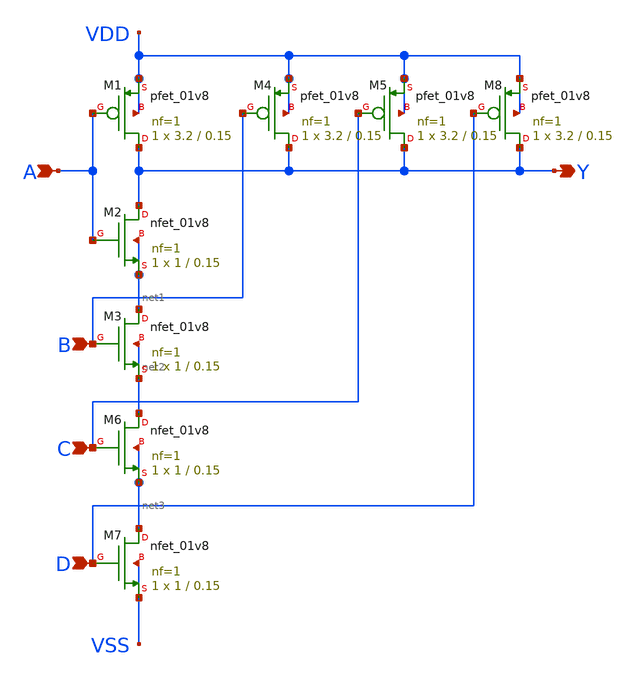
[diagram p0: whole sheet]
** sch_path: design/xschem/NAND/nand4.sch
**.subckt nand4 A Y B C D
*.ipin A
*.opin Y
*.ipin B
*.ipin C
*.ipin D
XM1 Y A VDD VDD sky130_fd_pr__pfet_01v8 L=0.15 W=3.2 nf=1 ad='int((nf+1)/2) * W/nf * 0.29' as='int((nf+2)/2) * W/nf * 0.29'
+ pd='2*int((nf+1)/2) * (W/nf + 0.29)' ps='2*int((nf+2)/2) * (W/nf + 0.29)' nrd='0.29 / W' nrs='0.29 / W'
+ sa=0 sb=0 sd=0 mult=1 m=1
XM2 Y A net1 net1 sky130_fd_pr__nfet_01v8 L=0.15 W=1 nf=1 ad='int((nf+1)/2) * W/nf * 0.29' as='int((nf+2)/2) * W/nf * 0.29'
+ pd='2*int((nf+1)/2) * (W/nf + 0.29)' ps='2*int((nf+2)/2) * (W/nf + 0.29)' nrd='0.29 / W' nrs='0.29 / W'
+ sa=0 sb=0 sd=0 mult=1 m=1
XM3 net1 B net2 net2 sky130_fd_pr__nfet_01v8 L=0.15 W=1 nf=1 ad='int((nf+1)/2) * W/nf * 0.29' as='int((nf+2)/2) * W/nf * 0.29'
+ pd='2*int((nf+1)/2) * (W/nf + 0.29)' ps='2*int((nf+2)/2) * (W/nf + 0.29)' nrd='0.29 / W' nrs='0.29 / W'
+ sa=0 sb=0 sd=0 mult=1 m=1
XM4 Y B VDD VDD sky130_fd_pr__pfet_01v8 L=0.15 W=3.2 nf=1 ad='int((nf+1)/2) * W/nf * 0.29' as='int((nf+2)/2) * W/nf * 0.29'
+ pd='2*int((nf+1)/2) * (W/nf + 0.29)' ps='2*int((nf+2)/2) * (W/nf + 0.29)' nrd='0.29 / W' nrs='0.29 / W'
+ sa=0 sb=0 sd=0 mult=1 m=1
XM5 Y C VDD VDD sky130_fd_pr__pfet_01v8 L=0.15 W=3.2 nf=1 ad='int((nf+1)/2) * W/nf * 0.29' as='int((nf+2)/2) * W/nf * 0.29'
+ pd='2*int((nf+1)/2) * (W/nf + 0.29)' ps='2*int((nf+2)/2) * (W/nf + 0.29)' nrd='0.29 / W' nrs='0.29 / W'
+ sa=0 sb=0 sd=0 mult=1 m=1
XM6 net2 C net3 net3 sky130_fd_pr__nfet_01v8 L=0.15 W=1 nf=1 ad='int((nf+1)/2) * W/nf * 0.29' as='int((nf+2)/2) * W/nf * 0.29'
+ pd='2*int((nf+1)/2) * (W/nf + 0.29)' ps='2*int((nf+2)/2) * (W/nf + 0.29)' nrd='0.29 / W' nrs='0.29 / W'
+ sa=0 sb=0 sd=0 mult=1 m=1
XM7 net3 D VSS VSS sky130_fd_pr__nfet_01v8 L=0.15 W=1 nf=1 ad='int((nf+1)/2) * W/nf * 0.29' as='int((nf+2)/2) * W/nf * 0.29'
+ pd='2*int((nf+1)/2) * (W/nf + 0.29)' ps='2*int((nf+2)/2) * (W/nf + 0.29)' nrd='0.29 / W' nrs='0.29 / W'
+ sa=0 sb=0 sd=0 mult=1 m=1
XM8 Y D VDD VDD sky130_fd_pr__pfet_01v8 L=0.15 W=3.2 nf=1 ad='int((nf+1)/2) * W/nf * 0.29' as='int((nf+2)/2) * W/nf * 0.29'
+ pd='2*int((nf+1)/2) * (W/nf + 0.29)' ps='2*int((nf+2)/2) * (W/nf + 0.29)' nrd='0.29 / W' nrs='0.29 / W'
+ sa=0 sb=0 sd=0 mult=1 m=1
**.ends
.end
